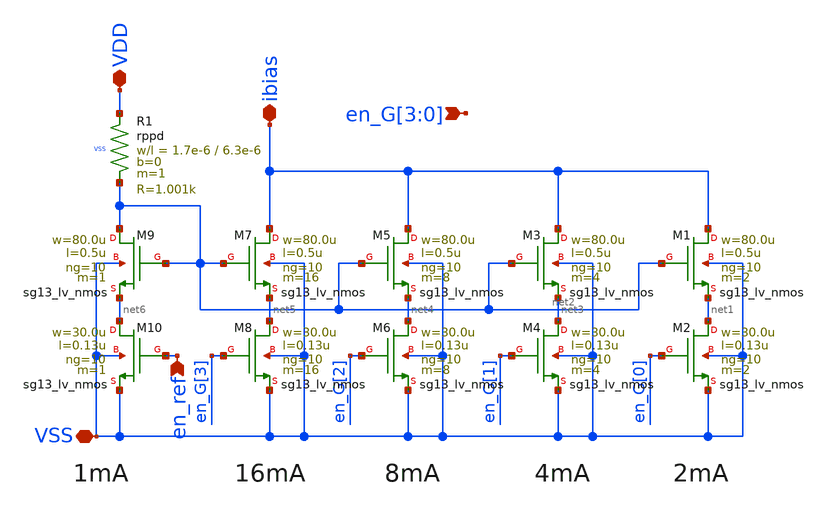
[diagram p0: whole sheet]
** sch_path: xschem/iruwbtx7_PA_currentMirror.sch
**.subckt iruwbtx7_PA_currentMirror ibias en_ref VSS VDD en_G[3],en_G[2],en_G[1],en_G[0]
*.iopin ibias
*.ipin en_ref
*.iopin VSS
*.iopin VDD
*.ipin en_G[3],en_G[2],en_G[1],en_G[0]
XM1 ibias net2 net1 VSS sg13_lv_nmos w=80.0u l=0.5u ng=10 m=2 mm_ok=1
XM2 net1 en_G[0] VSS VSS sg13_lv_nmos w=30.0u l=0.13u ng=10 m=2 mm_ok=1
XM3 ibias net2 net3 VSS sg13_lv_nmos w=80.0u l=0.5u ng=10 m=4 mm_ok=1
XM4 net3 en_G[1] VSS VSS sg13_lv_nmos w=30.0u l=0.13u ng=10 m=4 mm_ok=1
XM5 ibias net2 net4 VSS sg13_lv_nmos w=80.0u l=0.5u ng=10 m=8 mm_ok=1
XM6 net4 en_G[2] VSS VSS sg13_lv_nmos w=30.0u l=0.13u ng=10 m=8 mm_ok=1
XM7 ibias net2 net5 VSS sg13_lv_nmos w=80.0u l=0.5u ng=10 m=16 mm_ok=1
XM8 net5 en_G[3] VSS VSS sg13_lv_nmos w=30.0u l=0.13u ng=10 m=16 mm_ok=1
XM9 net2 net2 net6 VSS sg13_lv_nmos w=80.0u l=0.5u ng=10 m=1 mm_ok=1
XM10 net6 en_ref VSS VSS sg13_lv_nmos w=30.0u l=0.13u ng=10 m=1 mm_ok=1
XR1 VDD net2 VSS rppd w=1.7e-6 l=6.3e-6 m=1 b=0 mm_ok=1
**.ends
.end
